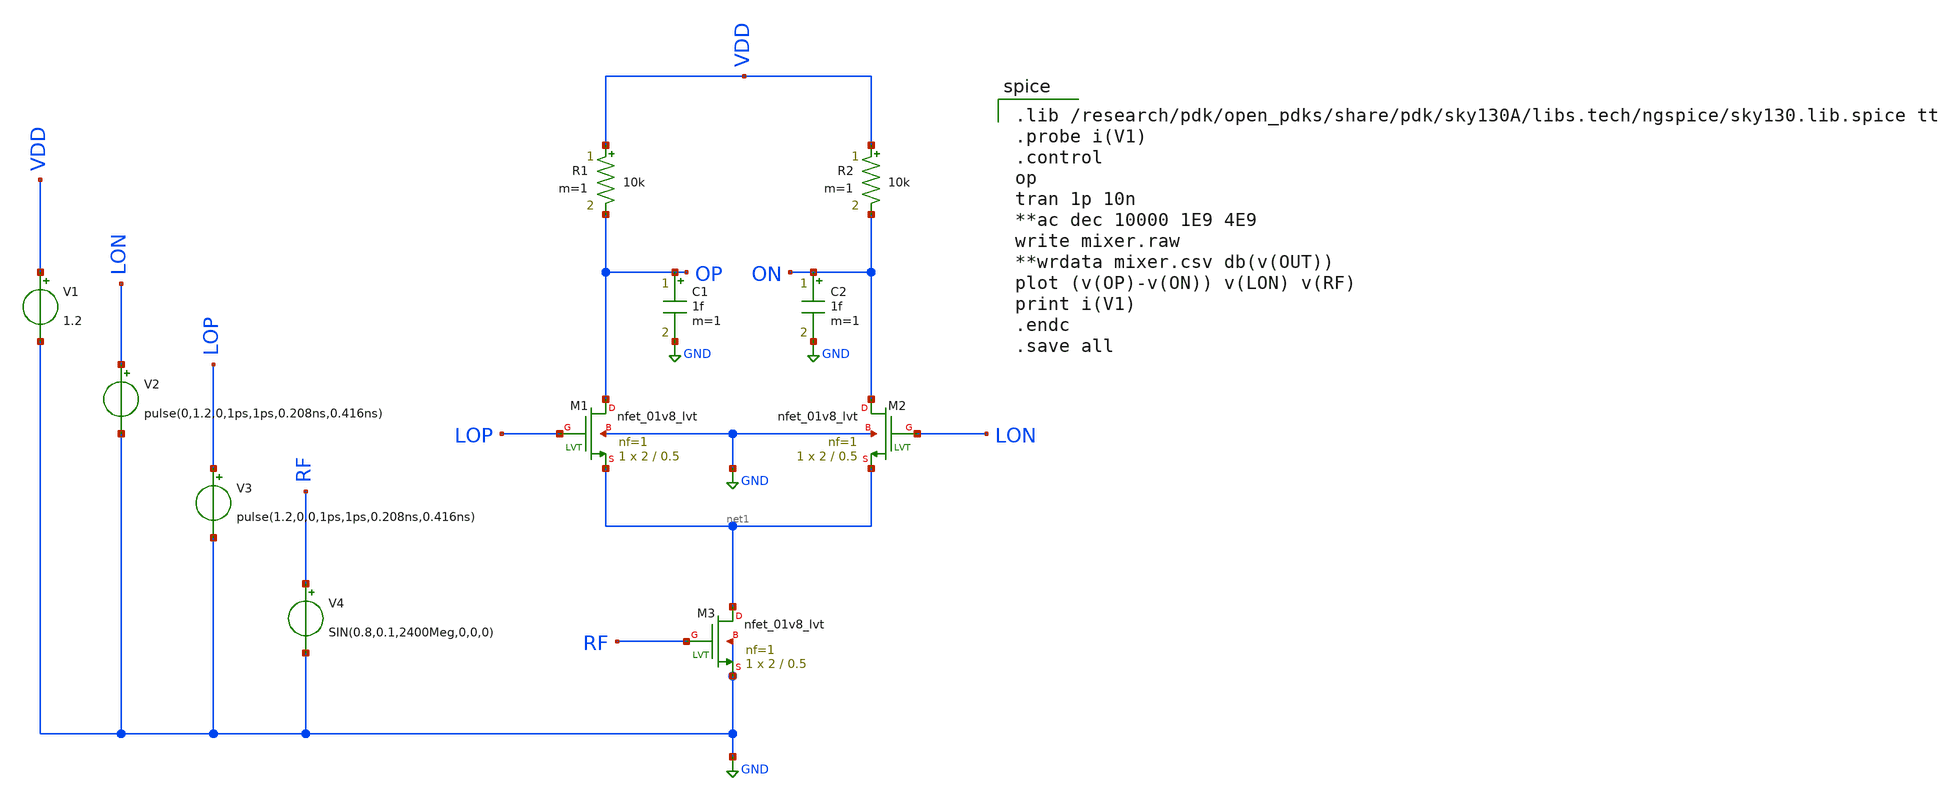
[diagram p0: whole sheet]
** sch_path: skywater_stuff/ECE631_RF_CMOS/mixer.sch
**.subckt mixer
XM1 OP LOP net1 GND sky130_fd_pr__nfet_01v8_lvt L=0.5 W=2 nf=1 ad='int((nf+1)/2) * W/nf * 0.29' as='int((nf+2)/2) * W/nf * 0.29'
+ pd='2*int((nf+1)/2) * (W/nf + 0.29)' ps='2*int((nf+2)/2) * (W/nf + 0.29)' nrd='0.29 / W' nrs='0.29 / W'
+ sa=0 sb=0 sd=0 mult=1 m=1
XM2 ON LON net1 GND sky130_fd_pr__nfet_01v8_lvt L=0.5 W=2 nf=1 ad='int((nf+1)/2) * W/nf * 0.29' as='int((nf+2)/2) * W/nf * 0.29'
+ pd='2*int((nf+1)/2) * (W/nf + 0.29)' ps='2*int((nf+2)/2) * (W/nf + 0.29)' nrd='0.29 / W' nrs='0.29 / W'
+ sa=0 sb=0 sd=0 mult=1 m=1
XM3 net1 RF GND GND sky130_fd_pr__nfet_01v8_lvt L=0.5 W=2 nf=1 ad='int((nf+1)/2) * W/nf * 0.29' as='int((nf+2)/2) * W/nf * 0.29'
+ pd='2*int((nf+1)/2) * (W/nf + 0.29)' ps='2*int((nf+2)/2) * (W/nf + 0.29)' nrd='0.29 / W' nrs='0.29 / W'
+ sa=0 sb=0 sd=0 mult=1 m=1
R1 VDD OP 10k m=1
R2 VDD ON 10k m=1
V1 VDD GND 1.2
V2 LON GND pulse(0,1.2,0,1ps,1ps,0.208ns,0.416ns)
V4 RF GND SIN(0.8,0.1,2400Meg,0,0,0)
V3 LOP GND pulse(1.2,0,0,1ps,1ps,0.208ns,0.416ns)
C2 ON GND 1f m=1
C1 OP GND 1f m=1
**** begin user architecture code

.lib /research/pdk/open_pdks/share/pdk/sky130A/libs.tech/ngspice/sky130.lib.spice tt
.probe i(V1)
.control
op
tran 1p 10n
**ac dec 10000 1E9 4E9
write mixer.raw
**wrdata mixer.csv db(v(OUT))
plot (v(OP)-v(ON)) v(LON) v(RF)
print i(V1)
.endc
.save all


**** end user architecture code
**.ends
.GLOBAL GND
.end
